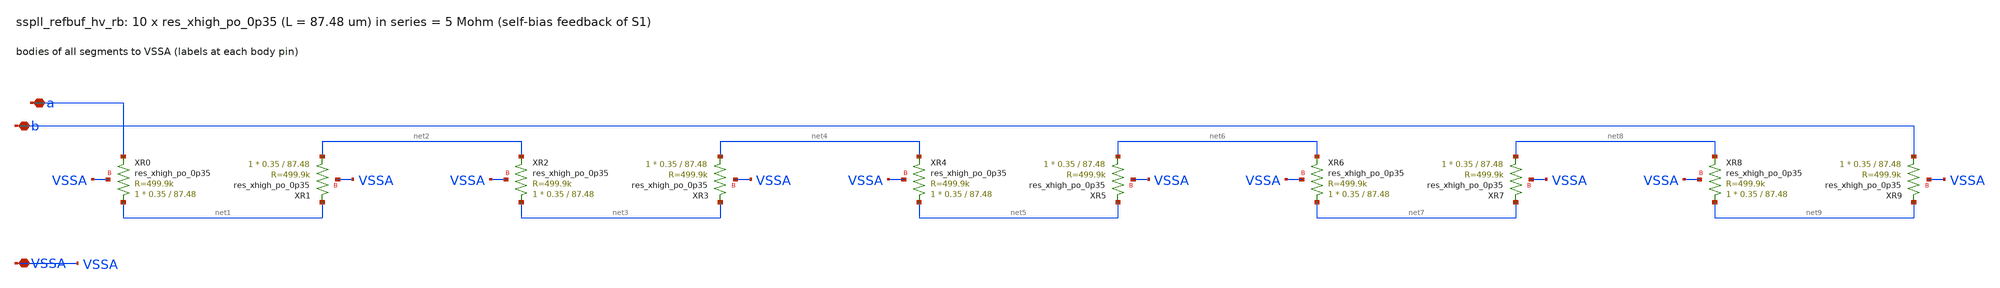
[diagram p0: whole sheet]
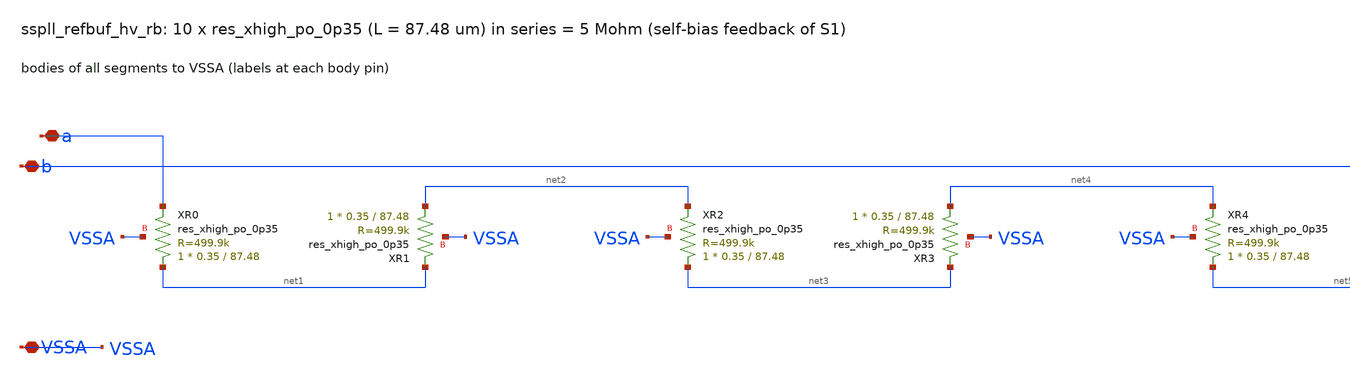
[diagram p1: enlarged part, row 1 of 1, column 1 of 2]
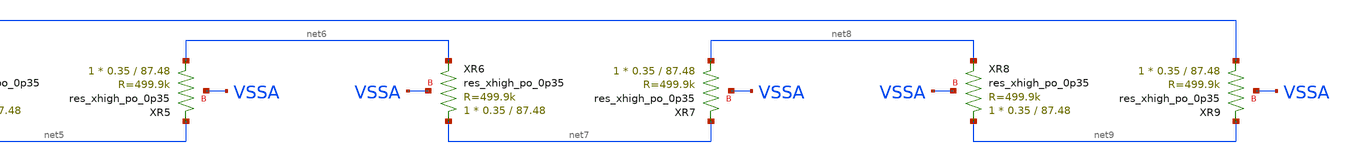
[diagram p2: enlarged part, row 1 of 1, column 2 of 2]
** sch_path: xschem/refbuf_hv/sspll_refbuf_hv_rb.sch
**.subckt sspll_refbuf_hv_rb a b VSSA
*.iopin a
*.iopin b
*.iopin VSSA
XXR0 net1 a VSSA sky130_fd_pr__res_xhigh_po_0p35 L=87.48 mult=1 m=1
XXR1 net2 net1 VSSA sky130_fd_pr__res_xhigh_po_0p35 L=87.48 mult=1 m=1
XXR2 net3 net2 VSSA sky130_fd_pr__res_xhigh_po_0p35 L=87.48 mult=1 m=1
XXR3 net4 net3 VSSA sky130_fd_pr__res_xhigh_po_0p35 L=87.48 mult=1 m=1
XXR4 net5 net4 VSSA sky130_fd_pr__res_xhigh_po_0p35 L=87.48 mult=1 m=1
XXR5 net6 net5 VSSA sky130_fd_pr__res_xhigh_po_0p35 L=87.48 mult=1 m=1
XXR6 net7 net6 VSSA sky130_fd_pr__res_xhigh_po_0p35 L=87.48 mult=1 m=1
XXR7 net8 net7 VSSA sky130_fd_pr__res_xhigh_po_0p35 L=87.48 mult=1 m=1
XXR8 net9 net8 VSSA sky130_fd_pr__res_xhigh_po_0p35 L=87.48 mult=1 m=1
XXR9 b net9 VSSA sky130_fd_pr__res_xhigh_po_0p35 L=87.48 mult=1 m=1
**.ends
.end
